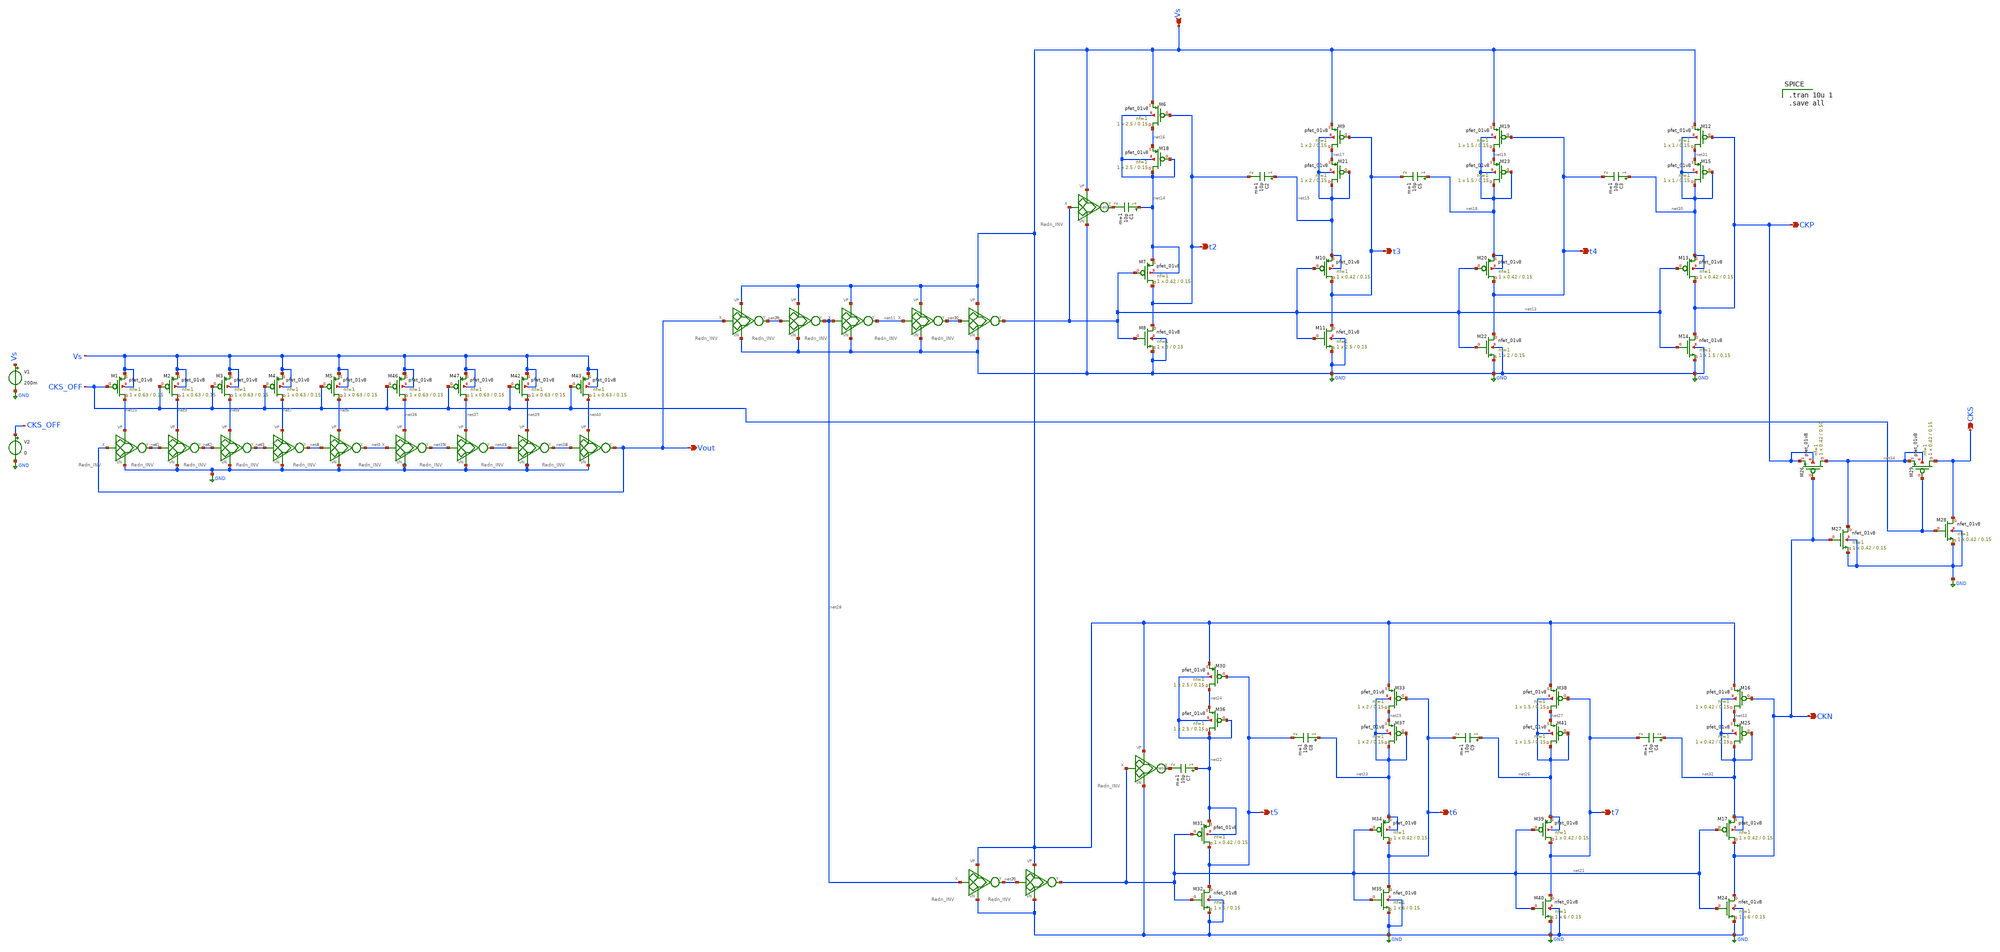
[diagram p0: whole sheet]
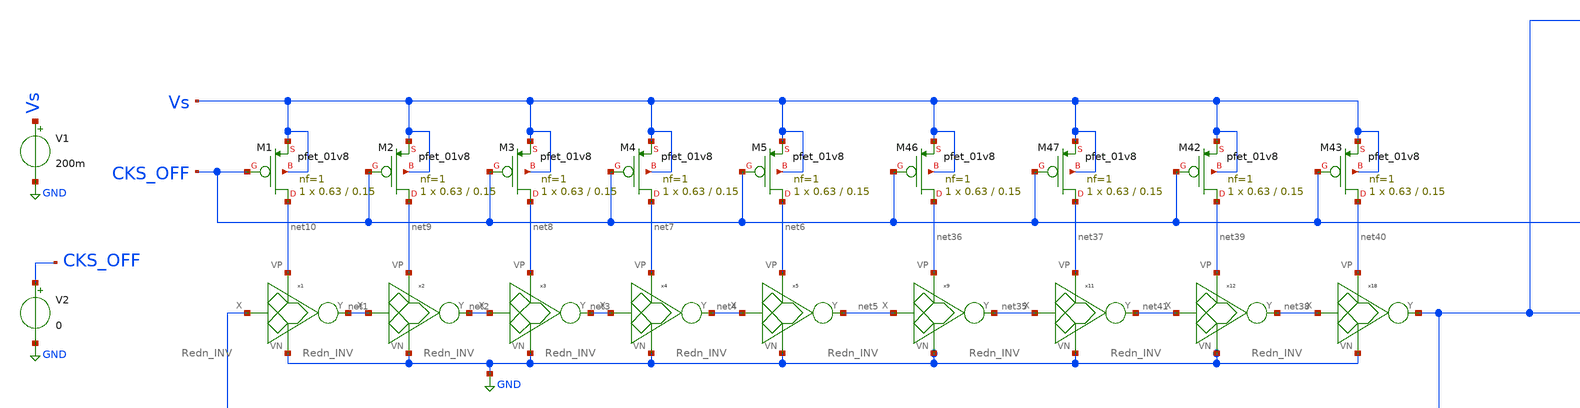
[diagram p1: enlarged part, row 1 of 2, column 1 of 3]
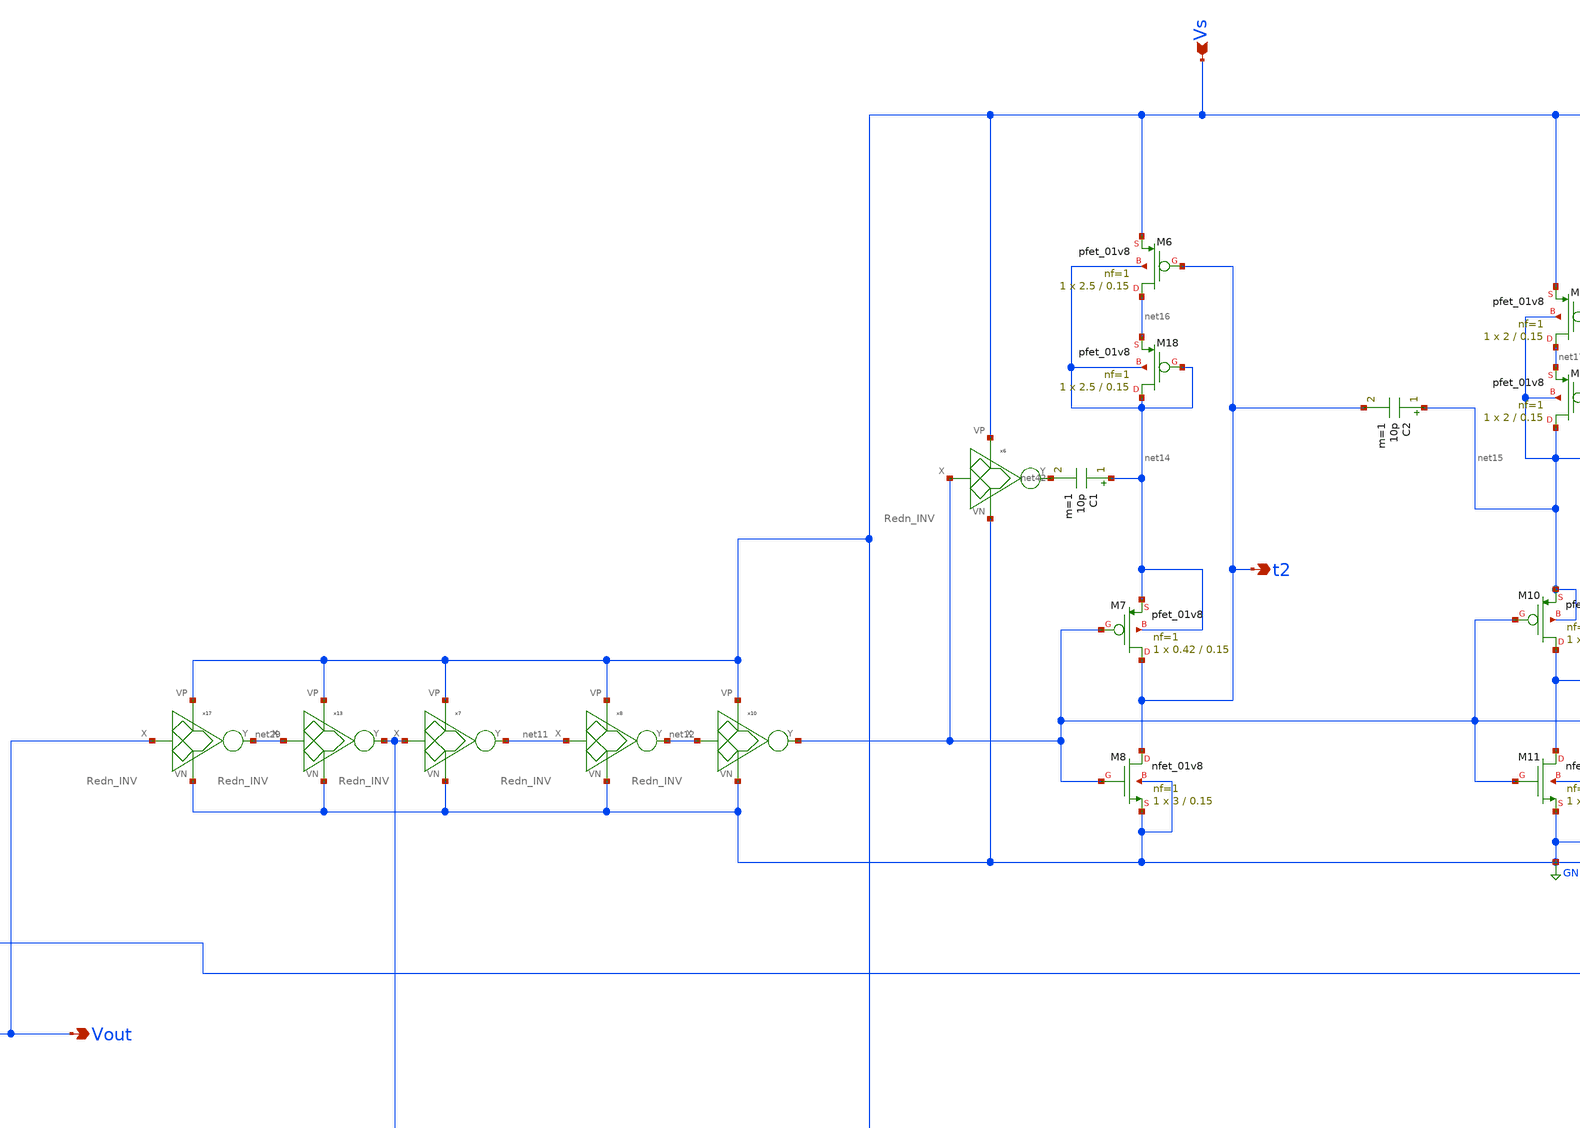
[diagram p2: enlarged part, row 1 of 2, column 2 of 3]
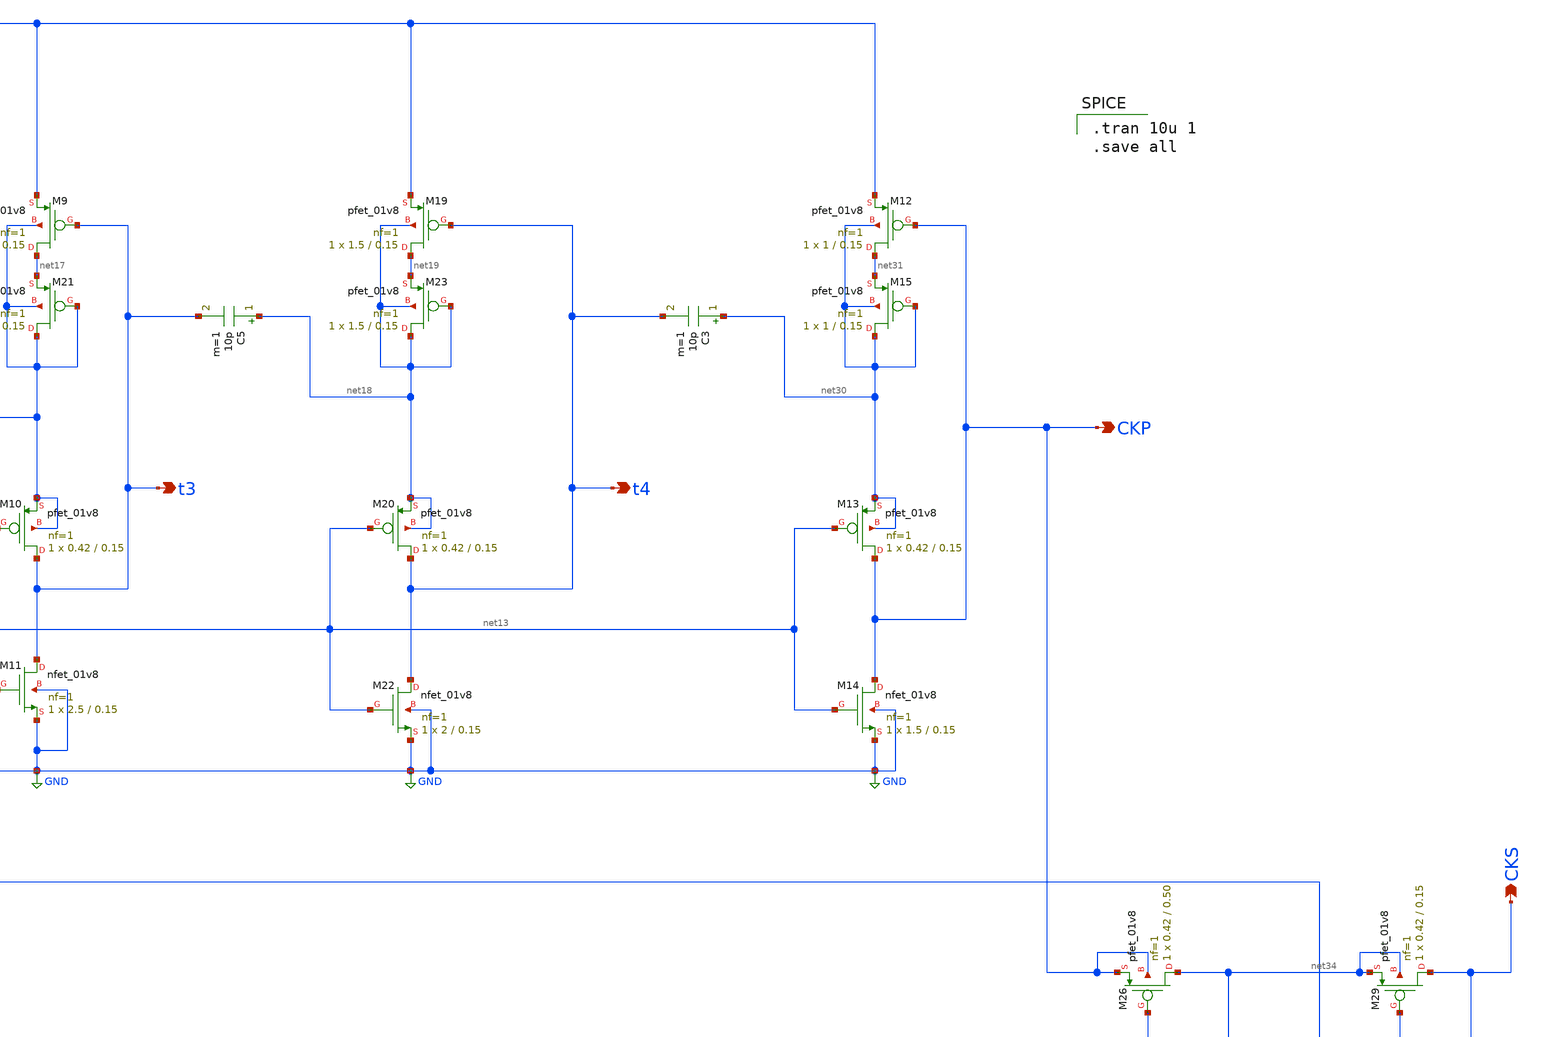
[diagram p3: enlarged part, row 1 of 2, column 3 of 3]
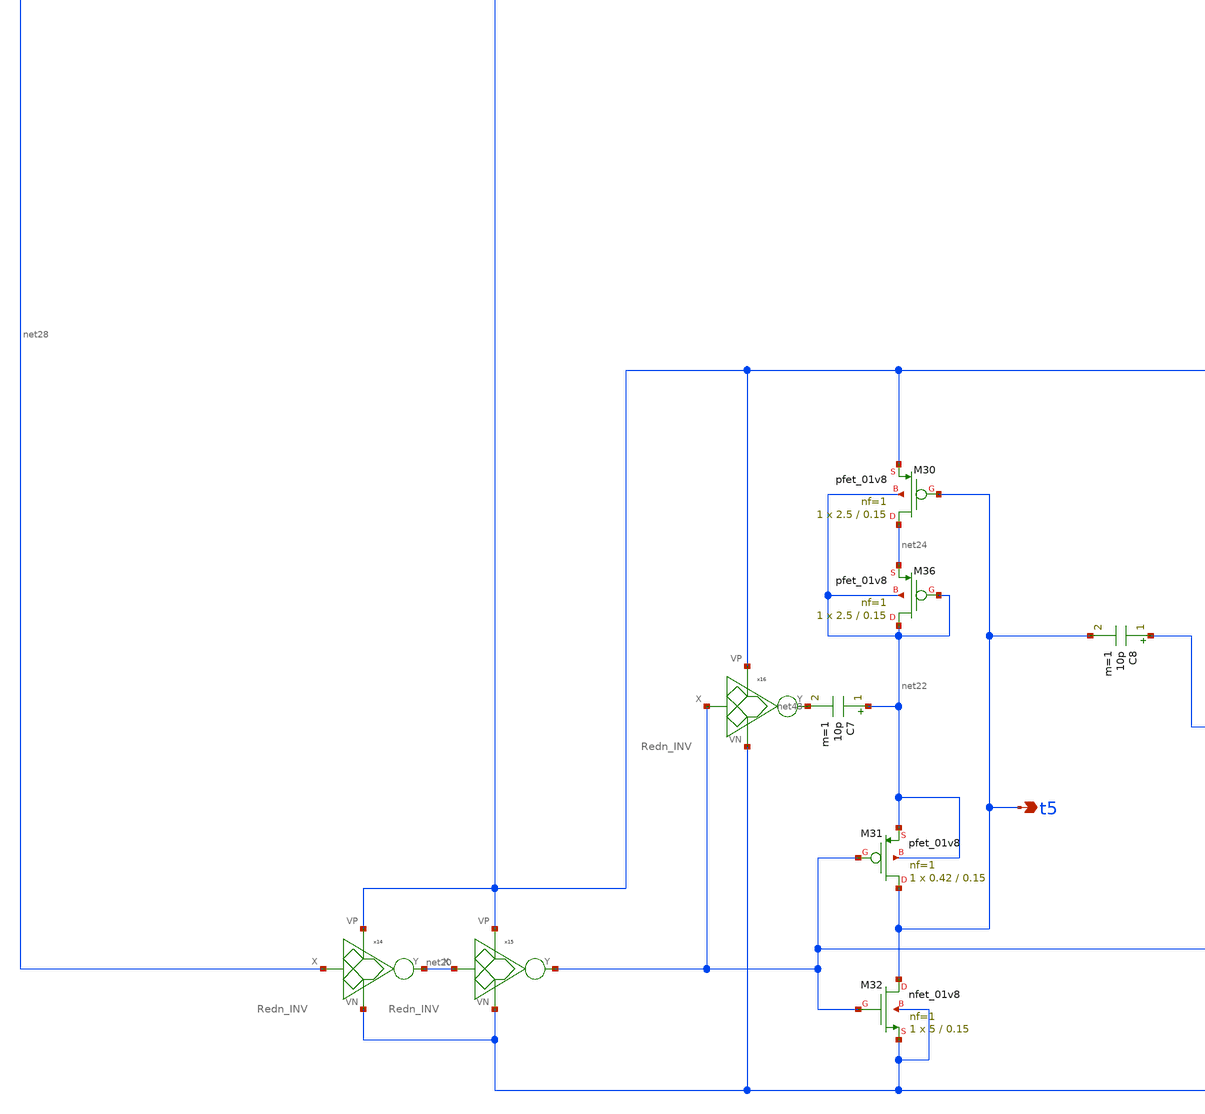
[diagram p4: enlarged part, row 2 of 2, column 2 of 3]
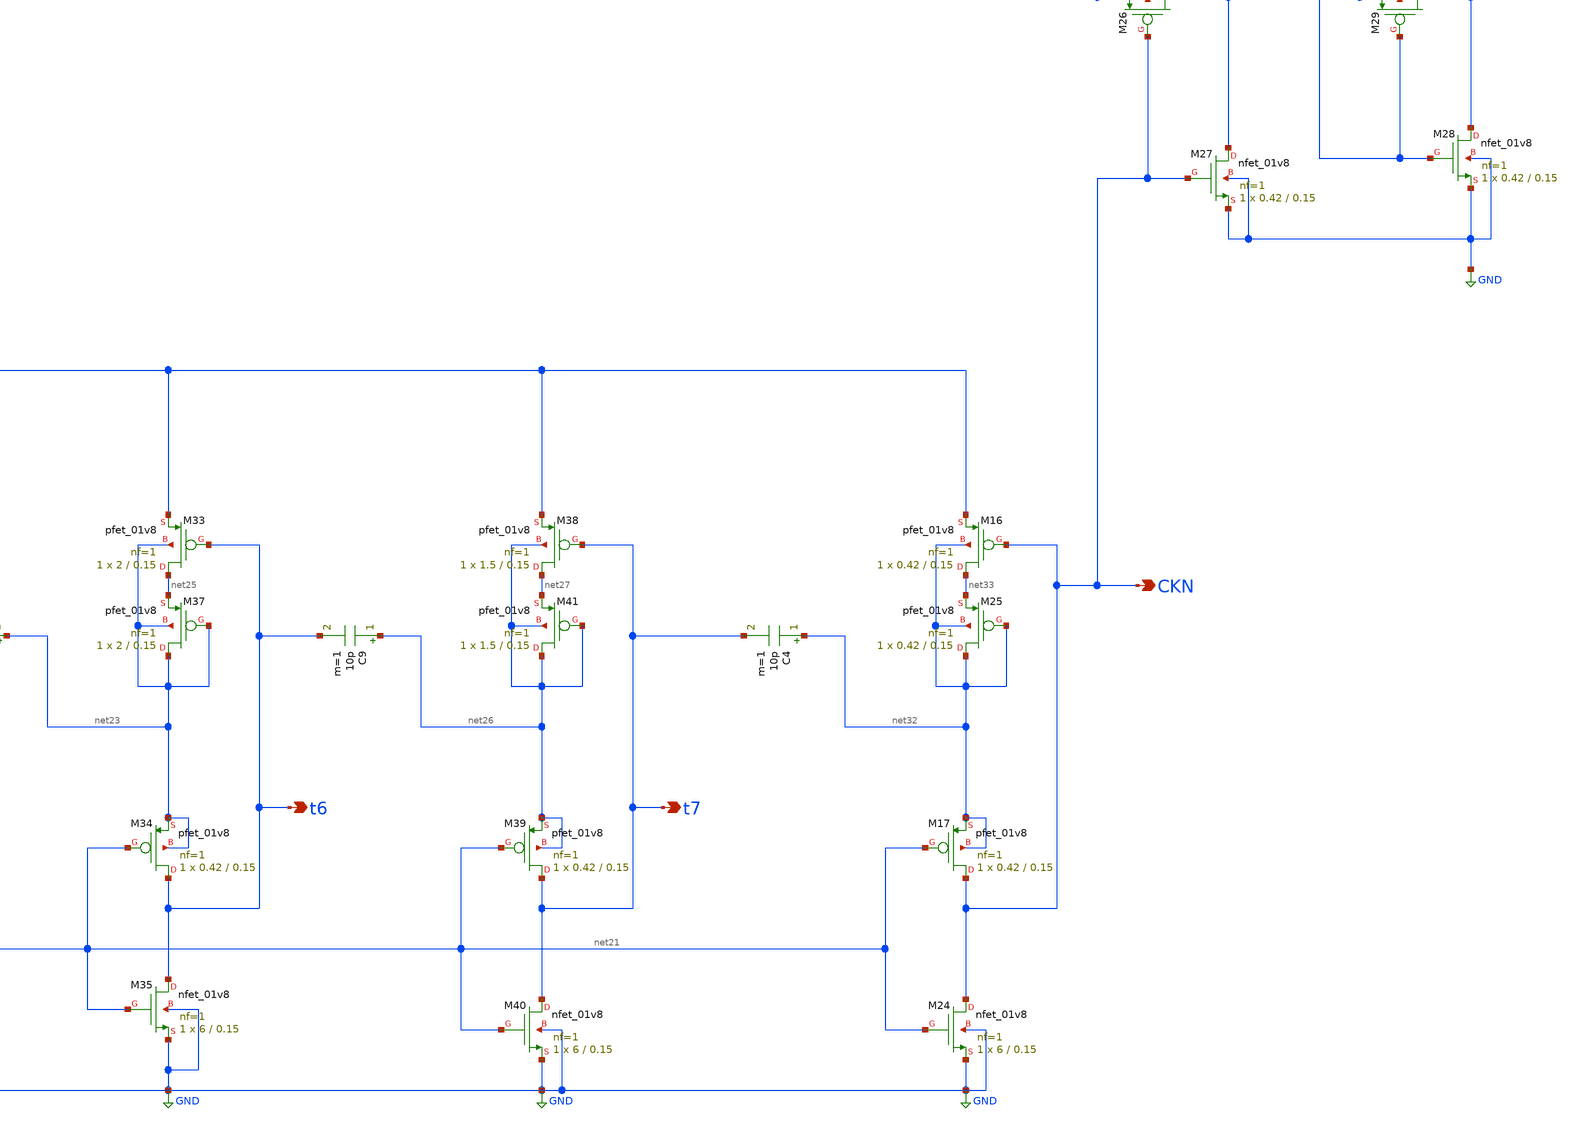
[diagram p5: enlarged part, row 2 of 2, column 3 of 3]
** sch_path: Blocks/Startup Converter/Startup_Cnv_2.sch
**.subckt Startup_Cnv_2 Vout Vs CKP CKN CKS t2 t3 t4 t5 t6 t7
*.opin Vout
*.ipin Vs
*.opin CKP
*.opin CKN
*.opin CKS
*.opin t2
*.opin t3
*.opin t4
*.opin t5
*.opin t6
*.opin t7
V1 Vs GND 200m
XM1 net10 CKS_OFF Vs Vs sky130_fd_pr__pfet_01v8 L=0.15 W=0.63 nf=1 ad='int((nf+1)/2) * W/nf * 0.29' as='int((nf+2)/2) * W/nf * 0.29'
+ pd='2*int((nf+1)/2) * (W/nf + 0.29)' ps='2*int((nf+2)/2) * (W/nf + 0.29)' nrd='0.29 / W' nrs='0.29 / W'
+ sa=0 sb=0 sd=0 mult=1 m=1
XM2 net9 CKS_OFF Vs Vs sky130_fd_pr__pfet_01v8 L=0.15 W=0.63 nf=1 ad='int((nf+1)/2) * W/nf * 0.29' as='int((nf+2)/2) * W/nf * 0.29'
+ pd='2*int((nf+1)/2) * (W/nf + 0.29)' ps='2*int((nf+2)/2) * (W/nf + 0.29)' nrd='0.29 / W' nrs='0.29 / W'
+ sa=0 sb=0 sd=0 mult=1 m=1
XM3 net8 CKS_OFF Vs Vs sky130_fd_pr__pfet_01v8 L=0.15 W=0.63 nf=1 ad='int((nf+1)/2) * W/nf * 0.29' as='int((nf+2)/2) * W/nf * 0.29'
+ pd='2*int((nf+1)/2) * (W/nf + 0.29)' ps='2*int((nf+2)/2) * (W/nf + 0.29)' nrd='0.29 / W' nrs='0.29 / W'
+ sa=0 sb=0 sd=0 mult=1 m=1
XM4 net7 CKS_OFF Vs Vs sky130_fd_pr__pfet_01v8 L=0.15 W=0.63 nf=1 ad='int((nf+1)/2) * W/nf * 0.29' as='int((nf+2)/2) * W/nf * 0.29'
+ pd='2*int((nf+1)/2) * (W/nf + 0.29)' ps='2*int((nf+2)/2) * (W/nf + 0.29)' nrd='0.29 / W' nrs='0.29 / W'
+ sa=0 sb=0 sd=0 mult=1 m=1
XM5 net6 CKS_OFF Vs Vs sky130_fd_pr__pfet_01v8 L=0.15 W=0.63 nf=1 ad='int((nf+1)/2) * W/nf * 0.29' as='int((nf+2)/2) * W/nf * 0.29'
+ pd='2*int((nf+1)/2) * (W/nf + 0.29)' ps='2*int((nf+2)/2) * (W/nf + 0.29)' nrd='0.29 / W' nrs='0.29 / W'
+ sa=0 sb=0 sd=0 mult=1 m=1
V2 CKS_OFF GND 0
x1 Vout net1 net10 GND Redn_INV
x2 net1 net2 net9 GND Redn_INV
x3 net2 net3 net8 GND Redn_INV
x4 net3 net4 net7 GND Redn_INV
x5 net4 net5 net6 GND Redn_INV
C1 net14 net42 10p m=1
XM6 net16 t2 Vs net14 sky130_fd_pr__pfet_01v8 L=0.15 W=2.5 nf=1 ad='int((nf+1)/2) * W/nf * 0.29' as='int((nf+2)/2) * W/nf * 0.29'
+ pd='2*int((nf+1)/2) * (W/nf + 0.29)' ps='2*int((nf+2)/2) * (W/nf + 0.29)' nrd='0.29 / W' nrs='0.29 / W'
+ sa=0 sb=0 sd=0 mult=1 m=1
XM7 t2 net13 net14 net14 sky130_fd_pr__pfet_01v8 L=0.15 W=0.42 nf=1 ad='int((nf+1)/2) * W/nf * 0.29'
+ as='int((nf+2)/2) * W/nf * 0.29' pd='2*int((nf+1)/2) * (W/nf + 0.29)' ps='2*int((nf+2)/2) * (W/nf + 0.29)'
+ nrd='0.29 / W' nrs='0.29 / W' sa=0 sb=0 sd=0 mult=1 m=1
XM8 t2 net13 GND GND sky130_fd_pr__nfet_01v8 L=0.15 W=3 nf=1 ad='int((nf+1)/2) * W/nf * 0.29' as='int((nf+2)/2) * W/nf * 0.29'
+ pd='2*int((nf+1)/2) * (W/nf + 0.29)' ps='2*int((nf+2)/2) * (W/nf + 0.29)' nrd='0.29 / W' nrs='0.29 / W'
+ sa=0 sb=0 sd=0 mult=1 m=1
XM9 net17 t3 Vs net15 sky130_fd_pr__pfet_01v8 L=0.15 W=2 nf=1 ad='int((nf+1)/2) * W/nf * 0.29' as='int((nf+2)/2) * W/nf * 0.29'
+ pd='2*int((nf+1)/2) * (W/nf + 0.29)' ps='2*int((nf+2)/2) * (W/nf + 0.29)' nrd='0.29 / W' nrs='0.29 / W'
+ sa=0 sb=0 sd=0 mult=1 m=1
XM10 t3 net13 net15 net15 sky130_fd_pr__pfet_01v8 L=0.15 W=0.42 nf=1 ad='int((nf+1)/2) * W/nf * 0.29'
+ as='int((nf+2)/2) * W/nf * 0.29' pd='2*int((nf+1)/2) * (W/nf + 0.29)' ps='2*int((nf+2)/2) * (W/nf + 0.29)'
+ nrd='0.29 / W' nrs='0.29 / W' sa=0 sb=0 sd=0 mult=1 m=1
XM11 t3 net13 GND GND sky130_fd_pr__nfet_01v8 L=0.15 W=2.5 nf=1 ad='int((nf+1)/2) * W/nf * 0.29' as='int((nf+2)/2) * W/nf * 0.29'
+ pd='2*int((nf+1)/2) * (W/nf + 0.29)' ps='2*int((nf+2)/2) * (W/nf + 0.29)' nrd='0.29 / W' nrs='0.29 / W'
+ sa=0 sb=0 sd=0 mult=1 m=1
XM18 net14 net14 net16 net14 sky130_fd_pr__pfet_01v8 L=0.15 W=2.5 nf=1 ad='int((nf+1)/2) * W/nf * 0.29'
+ as='int((nf+2)/2) * W/nf * 0.29' pd='2*int((nf+1)/2) * (W/nf + 0.29)' ps='2*int((nf+2)/2) * (W/nf + 0.29)'
+ nrd='0.29 / W' nrs='0.29 / W' sa=0 sb=0 sd=0 mult=1 m=1
XM21 net15 net15 net17 net15 sky130_fd_pr__pfet_01v8 L=0.15 W=2 nf=1 ad='int((nf+1)/2) * W/nf * 0.29'
+ as='int((nf+2)/2) * W/nf * 0.29' pd='2*int((nf+1)/2) * (W/nf + 0.29)' ps='2*int((nf+2)/2) * (W/nf + 0.29)'
+ nrd='0.29 / W' nrs='0.29 / W' sa=0 sb=0 sd=0 mult=1 m=1
C2 net15 t2 10p m=1
x7 net28 net11 Vs GND Redn_INV
x8 net11 net12 Vs GND Redn_INV
x10 net12 net13 Vs GND Redn_INV
x6 net13 net42 Vs GND Redn_INV
XM19 net19 t4 Vs net18 sky130_fd_pr__pfet_01v8 L=0.15 W=1.5 nf=1 ad='int((nf+1)/2) * W/nf * 0.29' as='int((nf+2)/2) * W/nf * 0.29'
+ pd='2*int((nf+1)/2) * (W/nf + 0.29)' ps='2*int((nf+2)/2) * (W/nf + 0.29)' nrd='0.29 / W' nrs='0.29 / W'
+ sa=0 sb=0 sd=0 mult=1 m=1
XM20 t4 net13 net18 net18 sky130_fd_pr__pfet_01v8 L=0.15 W=0.42 nf=1 ad='int((nf+1)/2) * W/nf * 0.29'
+ as='int((nf+2)/2) * W/nf * 0.29' pd='2*int((nf+1)/2) * (W/nf + 0.29)' ps='2*int((nf+2)/2) * (W/nf + 0.29)'
+ nrd='0.29 / W' nrs='0.29 / W' sa=0 sb=0 sd=0 mult=1 m=1
XM22 t4 net13 GND GND sky130_fd_pr__nfet_01v8 L=0.15 W=2 nf=1 ad='int((nf+1)/2) * W/nf * 0.29' as='int((nf+2)/2) * W/nf * 0.29'
+ pd='2*int((nf+1)/2) * (W/nf + 0.29)' ps='2*int((nf+2)/2) * (W/nf + 0.29)' nrd='0.29 / W' nrs='0.29 / W'
+ sa=0 sb=0 sd=0 mult=1 m=1
XM23 net18 net18 net19 net18 sky130_fd_pr__pfet_01v8 L=0.15 W=1.5 nf=1 ad='int((nf+1)/2) * W/nf * 0.29'
+ as='int((nf+2)/2) * W/nf * 0.29' pd='2*int((nf+1)/2) * (W/nf + 0.29)' ps='2*int((nf+2)/2) * (W/nf + 0.29)'
+ nrd='0.29 / W' nrs='0.29 / W' sa=0 sb=0 sd=0 mult=1 m=1
C5 net18 t3 10p m=1
C7 net22 net43 10p m=1
XM30 net24 t5 Vs net22 sky130_fd_pr__pfet_01v8 L=0.15 W=2.5 nf=1 ad='int((nf+1)/2) * W/nf * 0.29' as='int((nf+2)/2) * W/nf * 0.29'
+ pd='2*int((nf+1)/2) * (W/nf + 0.29)' ps='2*int((nf+2)/2) * (W/nf + 0.29)' nrd='0.29 / W' nrs='0.29 / W'
+ sa=0 sb=0 sd=0 mult=1 m=1
XM31 t5 net21 net22 net22 sky130_fd_pr__pfet_01v8 L=0.15 W=0.42 nf=1 ad='int((nf+1)/2) * W/nf * 0.29'
+ as='int((nf+2)/2) * W/nf * 0.29' pd='2*int((nf+1)/2) * (W/nf + 0.29)' ps='2*int((nf+2)/2) * (W/nf + 0.29)'
+ nrd='0.29 / W' nrs='0.29 / W' sa=0 sb=0 sd=0 mult=1 m=1
XM32 t5 net21 GND GND sky130_fd_pr__nfet_01v8 L=0.15 W=5 nf=1 ad='int((nf+1)/2) * W/nf * 0.29' as='int((nf+2)/2) * W/nf * 0.29'
+ pd='2*int((nf+1)/2) * (W/nf + 0.29)' ps='2*int((nf+2)/2) * (W/nf + 0.29)' nrd='0.29 / W' nrs='0.29 / W'
+ sa=0 sb=0 sd=0 mult=1 m=1
XM33 net25 t6 Vs net23 sky130_fd_pr__pfet_01v8 L=0.15 W=2 nf=1 ad='int((nf+1)/2) * W/nf * 0.29' as='int((nf+2)/2) * W/nf * 0.29'
+ pd='2*int((nf+1)/2) * (W/nf + 0.29)' ps='2*int((nf+2)/2) * (W/nf + 0.29)' nrd='0.29 / W' nrs='0.29 / W'
+ sa=0 sb=0 sd=0 mult=1 m=1
XM34 t6 net21 net23 net23 sky130_fd_pr__pfet_01v8 L=0.15 W=0.42 nf=1 ad='int((nf+1)/2) * W/nf * 0.29'
+ as='int((nf+2)/2) * W/nf * 0.29' pd='2*int((nf+1)/2) * (W/nf + 0.29)' ps='2*int((nf+2)/2) * (W/nf + 0.29)'
+ nrd='0.29 / W' nrs='0.29 / W' sa=0 sb=0 sd=0 mult=1 m=1
XM35 t6 net21 GND GND sky130_fd_pr__nfet_01v8 L=0.15 W=6 nf=1 ad='int((nf+1)/2) * W/nf * 0.29' as='int((nf+2)/2) * W/nf * 0.29'
+ pd='2*int((nf+1)/2) * (W/nf + 0.29)' ps='2*int((nf+2)/2) * (W/nf + 0.29)' nrd='0.29 / W' nrs='0.29 / W'
+ sa=0 sb=0 sd=0 mult=1 m=1
XM36 net22 net22 net24 net22 sky130_fd_pr__pfet_01v8 L=0.15 W=2.5 nf=1 ad='int((nf+1)/2) * W/nf * 0.29'
+ as='int((nf+2)/2) * W/nf * 0.29' pd='2*int((nf+1)/2) * (W/nf + 0.29)' ps='2*int((nf+2)/2) * (W/nf + 0.29)'
+ nrd='0.29 / W' nrs='0.29 / W' sa=0 sb=0 sd=0 mult=1 m=1
XM37 net23 net23 net25 net23 sky130_fd_pr__pfet_01v8 L=0.15 W=2 nf=1 ad='int((nf+1)/2) * W/nf * 0.29'
+ as='int((nf+2)/2) * W/nf * 0.29' pd='2*int((nf+1)/2) * (W/nf + 0.29)' ps='2*int((nf+2)/2) * (W/nf + 0.29)'
+ nrd='0.29 / W' nrs='0.29 / W' sa=0 sb=0 sd=0 mult=1 m=1
C8 net23 t5 10p m=1
x14 net28 net20 Vs GND Redn_INV
x15 net20 net21 Vs GND Redn_INV
x16 net21 net43 Vs GND Redn_INV
XM38 net27 t7 Vs net26 sky130_fd_pr__pfet_01v8 L=0.15 W=1.5 nf=1 ad='int((nf+1)/2) * W/nf * 0.29' as='int((nf+2)/2) * W/nf * 0.29'
+ pd='2*int((nf+1)/2) * (W/nf + 0.29)' ps='2*int((nf+2)/2) * (W/nf + 0.29)' nrd='0.29 / W' nrs='0.29 / W'
+ sa=0 sb=0 sd=0 mult=1 m=1
XM39 t7 net21 net26 net26 sky130_fd_pr__pfet_01v8 L=0.15 W=0.42 nf=1 ad='int((nf+1)/2) * W/nf * 0.29'
+ as='int((nf+2)/2) * W/nf * 0.29' pd='2*int((nf+1)/2) * (W/nf + 0.29)' ps='2*int((nf+2)/2) * (W/nf + 0.29)'
+ nrd='0.29 / W' nrs='0.29 / W' sa=0 sb=0 sd=0 mult=1 m=1
XM40 t7 net21 GND GND sky130_fd_pr__nfet_01v8 L=0.15 W=6 nf=1 ad='int((nf+1)/2) * W/nf * 0.29' as='int((nf+2)/2) * W/nf * 0.29'
+ pd='2*int((nf+1)/2) * (W/nf + 0.29)' ps='2*int((nf+2)/2) * (W/nf + 0.29)' nrd='0.29 / W' nrs='0.29 / W'
+ sa=0 sb=0 sd=0 mult=1 m=1
XM41 net26 net26 net27 net26 sky130_fd_pr__pfet_01v8 L=0.15 W=1.5 nf=1 ad='int((nf+1)/2) * W/nf * 0.29'
+ as='int((nf+2)/2) * W/nf * 0.29' pd='2*int((nf+1)/2) * (W/nf + 0.29)' ps='2*int((nf+2)/2) * (W/nf + 0.29)'
+ nrd='0.29 / W' nrs='0.29 / W' sa=0 sb=0 sd=0 mult=1 m=1
C9 net26 t6 10p m=1
x13 net29 net28 Vs GND Redn_INV
x17 Vout net29 Vs GND Redn_INV
XM12 net31 CKP Vs net30 sky130_fd_pr__pfet_01v8 L=0.15 W=1 nf=1 ad='int((nf+1)/2) * W/nf * 0.29' as='int((nf+2)/2) * W/nf * 0.29'
+ pd='2*int((nf+1)/2) * (W/nf + 0.29)' ps='2*int((nf+2)/2) * (W/nf + 0.29)' nrd='0.29 / W' nrs='0.29 / W'
+ sa=0 sb=0 sd=0 mult=1 m=1
XM13 CKP net13 net30 net30 sky130_fd_pr__pfet_01v8 L=0.15 W=0.42 nf=1 ad='int((nf+1)/2) * W/nf * 0.29'
+ as='int((nf+2)/2) * W/nf * 0.29' pd='2*int((nf+1)/2) * (W/nf + 0.29)' ps='2*int((nf+2)/2) * (W/nf + 0.29)'
+ nrd='0.29 / W' nrs='0.29 / W' sa=0 sb=0 sd=0 mult=1 m=1
XM14 CKP net13 GND GND sky130_fd_pr__nfet_01v8 L=0.15 W=1.5 nf=1 ad='int((nf+1)/2) * W/nf * 0.29' as='int((nf+2)/2) * W/nf * 0.29'
+ pd='2*int((nf+1)/2) * (W/nf + 0.29)' ps='2*int((nf+2)/2) * (W/nf + 0.29)' nrd='0.29 / W' nrs='0.29 / W'
+ sa=0 sb=0 sd=0 mult=1 m=1
XM15 net30 net30 net31 net30 sky130_fd_pr__pfet_01v8 L=0.15 W=1 nf=1 ad='int((nf+1)/2) * W/nf * 0.29'
+ as='int((nf+2)/2) * W/nf * 0.29' pd='2*int((nf+1)/2) * (W/nf + 0.29)' ps='2*int((nf+2)/2) * (W/nf + 0.29)'
+ nrd='0.29 / W' nrs='0.29 / W' sa=0 sb=0 sd=0 mult=1 m=1
C3 net30 t4 10p m=1
XM16 net33 CKN Vs net32 sky130_fd_pr__pfet_01v8 L=0.15 W=0.42 nf=1 ad='int((nf+1)/2) * W/nf * 0.29' as='int((nf+2)/2) * W/nf * 0.29'
+ pd='2*int((nf+1)/2) * (W/nf + 0.29)' ps='2*int((nf+2)/2) * (W/nf + 0.29)' nrd='0.29 / W' nrs='0.29 / W'
+ sa=0 sb=0 sd=0 mult=1 m=1
XM17 CKN net21 net32 net32 sky130_fd_pr__pfet_01v8 L=0.15 W=0.42 nf=1 ad='int((nf+1)/2) * W/nf * 0.29'
+ as='int((nf+2)/2) * W/nf * 0.29' pd='2*int((nf+1)/2) * (W/nf + 0.29)' ps='2*int((nf+2)/2) * (W/nf + 0.29)'
+ nrd='0.29 / W' nrs='0.29 / W' sa=0 sb=0 sd=0 mult=1 m=1
XM24 CKN net21 GND GND sky130_fd_pr__nfet_01v8 L=0.15 W=6 nf=1 ad='int((nf+1)/2) * W/nf * 0.29' as='int((nf+2)/2) * W/nf * 0.29'
+ pd='2*int((nf+1)/2) * (W/nf + 0.29)' ps='2*int((nf+2)/2) * (W/nf + 0.29)' nrd='0.29 / W' nrs='0.29 / W'
+ sa=0 sb=0 sd=0 mult=1 m=1
XM25 net32 net32 net33 net32 sky130_fd_pr__pfet_01v8 L=0.15 W=0.42 nf=1 ad='int((nf+1)/2) * W/nf * 0.29'
+ as='int((nf+2)/2) * W/nf * 0.29' pd='2*int((nf+1)/2) * (W/nf + 0.29)' ps='2*int((nf+2)/2) * (W/nf + 0.29)'
+ nrd='0.29 / W' nrs='0.29 / W' sa=0 sb=0 sd=0 mult=1 m=1
C4 net32 t7 10p m=1
XM26 net34 CKN CKP CKP sky130_fd_pr__pfet_01v8 L=0.50 W=0.42 nf=1 ad='int((nf+1)/2) * W/nf * 0.29' as='int((nf+2)/2) * W/nf * 0.29'
+ pd='2*int((nf+1)/2) * (W/nf + 0.29)' ps='2*int((nf+2)/2) * (W/nf + 0.29)' nrd='0.29 / W' nrs='0.29 / W'
+ sa=0 sb=0 sd=0 mult=1 m=1
XM27 net34 CKN GND GND sky130_fd_pr__nfet_01v8 L=0.15 W=0.42 nf=1 ad='int((nf+1)/2) * W/nf * 0.29' as='int((nf+2)/2) * W/nf * 0.29'
+ pd='2*int((nf+1)/2) * (W/nf + 0.29)' ps='2*int((nf+2)/2) * (W/nf + 0.29)' nrd='0.29 / W' nrs='0.29 / W'
+ sa=0 sb=0 sd=0 mult=1 m=1
XM28 CKS CKS_OFF GND GND sky130_fd_pr__nfet_01v8 L=0.15 W=0.42 nf=1 ad='int((nf+1)/2) * W/nf * 0.29'
+ as='int((nf+2)/2) * W/nf * 0.29' pd='2*int((nf+1)/2) * (W/nf + 0.29)' ps='2*int((nf+2)/2) * (W/nf + 0.29)'
+ nrd='0.29 / W' nrs='0.29 / W' sa=0 sb=0 sd=0 mult=1 m=1
XM29 CKS CKS_OFF net34 net34 sky130_fd_pr__pfet_01v8 L=0.15 W=0.42 nf=1 ad='int((nf+1)/2) * W/nf * 0.29'
+ as='int((nf+2)/2) * W/nf * 0.29' pd='2*int((nf+1)/2) * (W/nf + 0.29)' ps='2*int((nf+2)/2) * (W/nf + 0.29)'
+ nrd='0.29 / W' nrs='0.29 / W' sa=0 sb=0 sd=0 mult=1 m=1
x9 net5 net35 net36 GND Redn_INV
x11 net35 net41 net37 GND Redn_INV
XM46 net36 CKS_OFF Vs Vs sky130_fd_pr__pfet_01v8 L=0.15 W=0.63 nf=1 ad='int((nf+1)/2) * W/nf * 0.29'
+ as='int((nf+2)/2) * W/nf * 0.29' pd='2*int((nf+1)/2) * (W/nf + 0.29)' ps='2*int((nf+2)/2) * (W/nf + 0.29)'
+ nrd='0.29 / W' nrs='0.29 / W' sa=0 sb=0 sd=0 mult=1 m=1
XM47 net37 CKS_OFF Vs Vs sky130_fd_pr__pfet_01v8 L=0.15 W=0.63 nf=1 ad='int((nf+1)/2) * W/nf * 0.29'
+ as='int((nf+2)/2) * W/nf * 0.29' pd='2*int((nf+1)/2) * (W/nf + 0.29)' ps='2*int((nf+2)/2) * (W/nf + 0.29)'
+ nrd='0.29 / W' nrs='0.29 / W' sa=0 sb=0 sd=0 mult=1 m=1
x12 net41 net38 net39 GND Redn_INV
x18 net38 Vout net40 GND Redn_INV
XM42 net39 CKS_OFF Vs Vs sky130_fd_pr__pfet_01v8 L=0.15 W=0.63 nf=1 ad='int((nf+1)/2) * W/nf * 0.29'
+ as='int((nf+2)/2) * W/nf * 0.29' pd='2*int((nf+1)/2) * (W/nf + 0.29)' ps='2*int((nf+2)/2) * (W/nf + 0.29)'
+ nrd='0.29 / W' nrs='0.29 / W' sa=0 sb=0 sd=0 mult=1 m=1
XM43 net40 CKS_OFF Vs Vs sky130_fd_pr__pfet_01v8 L=0.15 W=0.63 nf=1 ad='int((nf+1)/2) * W/nf * 0.29'
+ as='int((nf+2)/2) * W/nf * 0.29' pd='2*int((nf+1)/2) * (W/nf + 0.29)' ps='2*int((nf+2)/2) * (W/nf + 0.29)'
+ nrd='0.29 / W' nrs='0.29 / W' sa=0 sb=0 sd=0 mult=1 m=1
**** begin user architecture code

** opencircuitdesign pdks install
.lib $::SKYWATER_MODELS/sky130.lib.spice tt



.tran 10u 1
.save all

**** end user architecture code
**.ends

* expanding   symbol:  component/Reduntant_Inverter/Redn_INV.sym # of pins=4
** sym_path: component/Reduntant_Inverter/Redn_INV.sym
** sch_path: component/Reduntant_Inverter/Redn_INV.sch
.subckt Redn_INV X Y VP VN
*.opin Y
*.ipin X
*.iopin VP
*.iopin VN
XM15 net4 X VN VN sky130_fd_pr__nfet_01v8_lvt L=0.15 W=1 nf=1 ad='int((nf+1)/2) * W/nf * 0.29' as='int((nf+2)/2) * W/nf * 0.29'
+ pd='2*int((nf+1)/2) * (W/nf + 0.29)' ps='2*int((nf+2)/2) * (W/nf + 0.29)' nrd='0.29 / W' nrs='0.29 / W'
+ sa=0 sb=0 sd=0 mult=1 m=1
XM1 net5 X net3 VN sky130_fd_pr__nfet_01v8_lvt L=0.15 W=3.25 nf=1 ad='int((nf+1)/2) * W/nf * 0.29' as='int((nf+2)/2) * W/nf * 0.29'
+ pd='2*int((nf+1)/2) * (W/nf + 0.29)' ps='2*int((nf+2)/2) * (W/nf + 0.29)' nrd='0.29 / W' nrs='0.29 / W'
+ sa=0 sb=0 sd=0 mult=1 m=1
XM16 Y X net6 VN sky130_fd_pr__nfet_01v8_lvt L=0.15 W=6.5 nf=1 ad='int((nf+1)/2) * W/nf * 0.29' as='int((nf+2)/2) * W/nf * 0.29'
+ pd='2*int((nf+1)/2) * (W/nf + 0.29)' ps='2*int((nf+2)/2) * (W/nf + 0.29)' nrd='0.29 / W' nrs='0.29 / W'
+ sa=0 sb=0 sd=0 mult=1 m=1
XM17 net3 X VN VN sky130_fd_pr__nfet_01v8_lvt L=0.15 W=3.25 nf=1 ad='int((nf+1)/2) * W/nf * 0.29' as='int((nf+2)/2) * W/nf * 0.29'
+ pd='2*int((nf+1)/2) * (W/nf + 0.29)' ps='2*int((nf+2)/2) * (W/nf + 0.29)' nrd='0.29 / W' nrs='0.29 / W'
+ sa=0 sb=0 sd=0 mult=1 m=1
XM18 net2 X VN VN sky130_fd_pr__nfet_01v8_lvt L=0.15 W=1.5 nf=1 ad='int((nf+1)/2) * W/nf * 0.29' as='int((nf+2)/2) * W/nf * 0.29'
+ pd='2*int((nf+1)/2) * (W/nf + 0.29)' ps='2*int((nf+2)/2) * (W/nf + 0.29)' nrd='0.29 / W' nrs='0.29 / W'
+ sa=0 sb=0 sd=0 mult=1 m=1
XM19 net1 X VN VN sky130_fd_pr__nfet_01v8_lvt L=0.15 W=6.5 nf=1 ad='int((nf+1)/2) * W/nf * 0.29' as='int((nf+2)/2) * W/nf * 0.29'
+ pd='2*int((nf+1)/2) * (W/nf + 0.29)' ps='2*int((nf+2)/2) * (W/nf + 0.29)' nrd='0.29 / W' nrs='0.29 / W'
+ sa=0 sb=0 sd=0 mult=1 m=1
XM20 net6 X net1 VN sky130_fd_pr__nfet_01v8_lvt L=0.15 W=6.5 nf=1 ad='int((nf+1)/2) * W/nf * 0.29' as='int((nf+2)/2) * W/nf * 0.29'
+ pd='2*int((nf+1)/2) * (W/nf + 0.29)' ps='2*int((nf+2)/2) * (W/nf + 0.29)' nrd='0.29 / W' nrs='0.29 / W'
+ sa=0 sb=0 sd=0 mult=1 m=1
XM2 net4 X VP VP sky130_fd_pr__pfet_01v8 L=0.15 W=10 nf=1 ad='int((nf+1)/2) * W/nf * 0.29' as='int((nf+2)/2) * W/nf * 0.29'
+ pd='2*int((nf+1)/2) * (W/nf + 0.29)' ps='2*int((nf+2)/2) * (W/nf + 0.29)' nrd='0.29 / W' nrs='0.29 / W'
+ sa=0 sb=0 sd=0 mult=1 m=1
XM5 net5 X net4 net4 sky130_fd_pr__pfet_01v8 L=0.15 W=10 nf=1 ad='int((nf+1)/2) * W/nf * 0.29' as='int((nf+2)/2) * W/nf * 0.29'
+ pd='2*int((nf+1)/2) * (W/nf + 0.29)' ps='2*int((nf+2)/2) * (W/nf + 0.29)' nrd='0.29 / W' nrs='0.29 / W'
+ sa=0 sb=0 sd=0 mult=1 m=1
XM6 Y X net5 VP sky130_fd_pr__pfet_01v8 L=0.15 W=10 nf=1 ad='int((nf+1)/2) * W/nf * 0.29' as='int((nf+2)/2) * W/nf * 0.29'
+ pd='2*int((nf+1)/2) * (W/nf + 0.29)' ps='2*int((nf+2)/2) * (W/nf + 0.29)' nrd='0.29 / W' nrs='0.29 / W'
+ sa=0 sb=0 sd=0 mult=1 m=1
XM8 net3 X VP VP sky130_fd_pr__pfet_01v8 L=0.15 W=2 nf=1 ad='int((nf+1)/2) * W/nf * 0.29' as='int((nf+2)/2) * W/nf * 0.29'
+ pd='2*int((nf+1)/2) * (W/nf + 0.29)' ps='2*int((nf+2)/2) * (W/nf + 0.29)' nrd='0.29 / W' nrs='0.29 / W'
+ sa=0 sb=0 sd=0 mult=1 m=1
XM12 net2 X VP VP sky130_fd_pr__pfet_01v8 L=0.15 W=5 nf=1 ad='int((nf+1)/2) * W/nf * 0.29' as='int((nf+2)/2) * W/nf * 0.29'
+ pd='2*int((nf+1)/2) * (W/nf + 0.29)' ps='2*int((nf+2)/2) * (W/nf + 0.29)' nrd='0.29 / W' nrs='0.29 / W'
+ sa=0 sb=0 sd=0 mult=1 m=1
XM14 net6 X net2 VP sky130_fd_pr__pfet_01v8 L=0.15 W=5 nf=1 ad='int((nf+1)/2) * W/nf * 0.29' as='int((nf+2)/2) * W/nf * 0.29'
+ pd='2*int((nf+1)/2) * (W/nf + 0.29)' ps='2*int((nf+2)/2) * (W/nf + 0.29)' nrd='0.29 / W' nrs='0.29 / W'
+ sa=0 sb=0 sd=0 mult=1 m=1
XM21 net1 X VP VP sky130_fd_pr__pfet_01v8 L=0.15 W=1.5 nf=1 ad='int((nf+1)/2) * W/nf * 0.29' as='int((nf+2)/2) * W/nf * 0.29'
+ pd='2*int((nf+1)/2) * (W/nf + 0.29)' ps='2*int((nf+2)/2) * (W/nf + 0.29)' nrd='0.29 / W' nrs='0.29 / W'
+ sa=0 sb=0 sd=0 mult=1 m=1
.ends

.GLOBAL GND
.end
